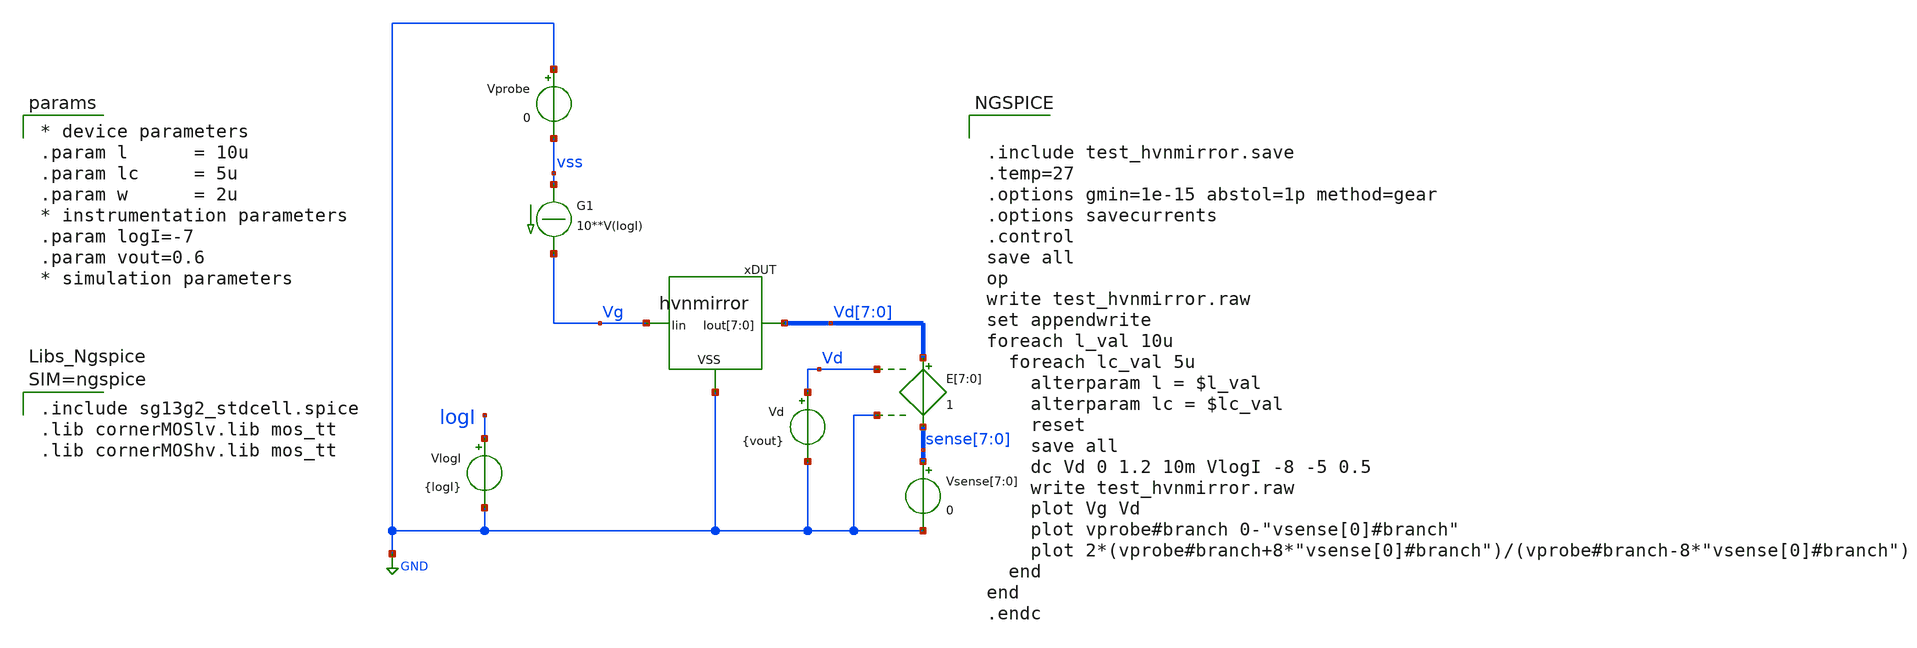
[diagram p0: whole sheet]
** sch_path: xschem/test_hvnmirror.sch
**.subckt test_hvnmirror
Vprobe GND vss 0
.save i(vprobe)
G1 vss Vg CUR=' 10**V(logI) '
VlogI logI GND {logI}
.save i(vlogi)
xDUT Vg Vd[7] Vd[6] Vd[5] Vd[4] Vd[3] Vd[2] Vd[1] Vd[0] GND hvnmirror
Vd Vd GND {vout}
.save i(vd)
E[7] Vd[7] sense[7] Vd GND 1
E[6] Vd[6] sense[6] Vd GND 1
E[5] Vd[5] sense[5] Vd GND 1
E[4] Vd[4] sense[4] Vd GND 1
E[3] Vd[3] sense[3] Vd GND 1
E[2] Vd[2] sense[2] Vd GND 1
E[1] Vd[1] sense[1] Vd GND 1
E[0] Vd[0] sense[0] Vd GND 1
Vsense[7] sense[7] GND 0
Vsense[6] sense[6] GND 0
Vsense[5] sense[5] GND 0
Vsense[4] sense[4] GND 0
Vsense[3] sense[3] GND 0
Vsense[2] sense[2] GND 0
Vsense[1] sense[1] GND 0
Vsense[0] sense[0] GND 0
.save i(vsense[7])
.save i(vsense[6])
.save i(vsense[5])
.save i(vsense[4])
.save i(vsense[3])
.save i(vsense[2])
.save i(vsense[1])
.save i(vsense[0])
**** begin user architecture code


.include sg13g2_stdcell.spice
.lib cornerMOSlv.lib mos_tt
.lib cornerMOShv.lib mos_tt



* device parameters
.param l      = 10u
.param lc     = 5u
.param w      = 2u
* instrumentation parameters
.param logI=-7
.param vout=0.6
* simulation parameters




.include test_hvnmirror.save
.temp=27
.options gmin=1e-15 abstol=1p method=gear
.options savecurrents
.control
save all
op
write test_hvnmirror.raw
set appendwrite
foreach l_val 10u
  foreach lc_val 5u
    alterparam l = $l_val
    alterparam lc = $lc_val
    reset
    save all
    dc Vd 0 1.2 10m VlogI -8 -5 0.5
    write test_hvnmirror.raw
    plot Vg Vd
    plot vprobe#branch 0-"vsense[0]#branch"
    plot 2*(vprobe#branch+8*"vsense[0]#branch")/(vprobe#branch-8*"vsense[0]#branch")
  end
end
.endc


**** end user architecture code
**.ends

* expanding   symbol:  hvnmirror.sym # of pins=3
** sym_path: xschem/hvnmirror.sym
** sch_path: xschem/hvnmirror.sch
.subckt hvnmirror Iin Iout[7] Iout[6] Iout[5] Iout[4] Iout[3] Iout[2] Iout[1] Iout[0] VSS
*.iopin VSS
*.iopin Iin
*.iopin Iout[0]
*.iopin Iout[1]
*.iopin Iout[2]
*.iopin Iout[3]
*.iopin Iout[4]
*.iopin Iout[5]
*.iopin Iout[6]
*.iopin Iout[7]
XM2[7] vd_in[7] Iin VSS VSS sg13_hv_nmos w=2u l=10u ng=1 m=1 mm_ok=1
XM2[6] vd_in[6] Iin VSS VSS sg13_hv_nmos w=2u l=10u ng=1 m=1 mm_ok=1
XM2[5] vd_in[5] Iin VSS VSS sg13_hv_nmos w=2u l=10u ng=1 m=1 mm_ok=1
XM2[4] vd_in[4] Iin VSS VSS sg13_hv_nmos w=2u l=10u ng=1 m=1 mm_ok=1
XM2[3] vd_in[3] Iin VSS VSS sg13_hv_nmos w=2u l=10u ng=1 m=1 mm_ok=1
XM2[2] vd_in[2] Iin VSS VSS sg13_hv_nmos w=2u l=10u ng=1 m=1 mm_ok=1
XM2[1] vd_in[1] Iin VSS VSS sg13_hv_nmos w=2u l=10u ng=1 m=1 mm_ok=1
XM2[0] vd_in[0] Iin VSS VSS sg13_hv_nmos w=2u l=10u ng=1 m=1 mm_ok=1
XM3 vd_0 Iin VSS VSS sg13_hv_nmos w=2u l=10u ng=1 m=1 mm_ok=1
XM1[7] Iin Iin vd_in[7] VSS sg13_hv_nmos w=2u l=5u ng=1 m=1 mm_ok=1
XM1[6] Iin Iin vd_in[6] VSS sg13_hv_nmos w=2u l=5u ng=1 m=1 mm_ok=1
XM1[5] Iin Iin vd_in[5] VSS sg13_hv_nmos w=2u l=5u ng=1 m=1 mm_ok=1
XM1[4] Iin Iin vd_in[4] VSS sg13_hv_nmos w=2u l=5u ng=1 m=1 mm_ok=1
XM1[3] Iin Iin vd_in[3] VSS sg13_hv_nmos w=2u l=5u ng=1 m=1 mm_ok=1
XM1[2] Iin Iin vd_in[2] VSS sg13_hv_nmos w=2u l=5u ng=1 m=1 mm_ok=1
XM1[1] Iin Iin vd_in[1] VSS sg13_hv_nmos w=2u l=5u ng=1 m=1 mm_ok=1
XM1[0] Iin Iin vd_in[0] VSS sg13_hv_nmos w=2u l=5u ng=1 m=1 mm_ok=1
XM4 Iout[0] Iin vd_0 VSS sg13_hv_nmos w=2u l=5u ng=1 m=1 mm_ok=1
XM5 vd_1 Iin VSS VSS sg13_hv_nmos w=2u l=10u ng=1 m=1 mm_ok=1
XM6 Iout[1] Iin vd_1 VSS sg13_hv_nmos w=2u l=5u ng=1 m=1 mm_ok=1
XM7 vd_2 Iin VSS VSS sg13_hv_nmos w=2u l=10u ng=1 m=1 mm_ok=1
XM8 Iout[2] Iin vd_2 VSS sg13_hv_nmos w=2u l=5u ng=1 m=1 mm_ok=1
XM9 vd_3 Iin VSS VSS sg13_hv_nmos w=2u l=10u ng=1 m=1 mm_ok=1
XM10 Iout[3] Iin vd_3 VSS sg13_hv_nmos w=2u l=5u ng=1 m=1 mm_ok=1
XM11 vd_4 Iin VSS VSS sg13_hv_nmos w=2u l=10u ng=1 m=1 mm_ok=1
XM12 Iout[4] Iin vd_4 VSS sg13_hv_nmos w=2u l=5u ng=1 m=1 mm_ok=1
XM13 vd_5 Iin VSS VSS sg13_hv_nmos w=2u l=10u ng=1 m=1 mm_ok=1
XM14 Iout[5] Iin vd_5 VSS sg13_hv_nmos w=2u l=5u ng=1 m=1 mm_ok=1
XM15 vd_6 Iin VSS VSS sg13_hv_nmos w=2u l=10u ng=1 m=1 mm_ok=1
XM16 Iout[6] Iin vd_6 VSS sg13_hv_nmos w=2u l=5u ng=1 m=1 mm_ok=1
XM17 vd_7 Iin VSS VSS sg13_hv_nmos w=2u l=10u ng=1 m=1 mm_ok=1
XM18 Iout[7] Iin vd_7 VSS sg13_hv_nmos w=2u l=5u ng=1 m=1 mm_ok=1
.ends

.GLOBAL GND
.end
